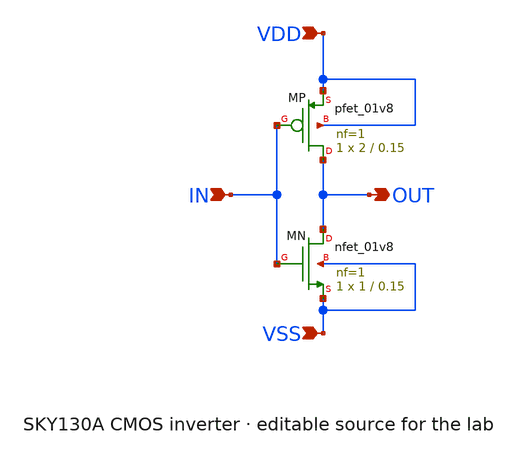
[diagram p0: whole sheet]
** sch_path: examples/sky130_inverter/inverter.sch
**.subckt inverter IN OUT VDD VSS
*.ipin IN
*.opin OUT
*.ipin VDD
*.ipin VSS
XMN OUT IN VSS VSS sky130_fd_pr__nfet_01v8 L=0.15 W=1 nf=1 ad=0.29 as=0.29 pd=2.58 ps=2.58 nrd=0
+ nrs=0 sa=0 sb=0 sd=0 mult=1 m=1
XMP OUT IN VDD VDD sky130_fd_pr__pfet_01v8 L=0.15 W=2 nf=1 ad=0.58 as=0.58 pd=4.58 ps=4.58 nrd=0
+ nrs=0 sa=0 sb=0 sd=0 mult=1 m=1
**.ends
.end
